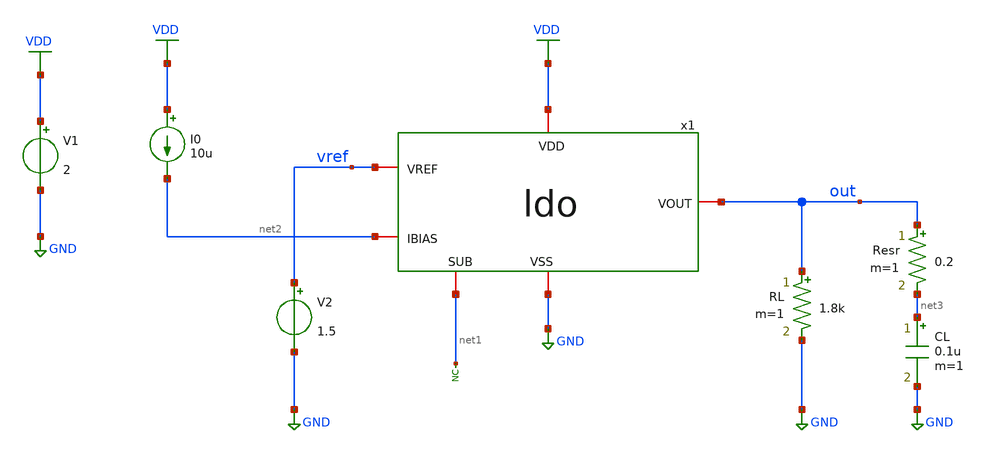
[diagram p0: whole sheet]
** sch_path: designs/libs/tb_ldo/tb_ldo/tb_ldo/tb_ldo_noise/tb_ldo_noise.sch
**.subckt tb_ldo_noise
* noconn #net1
RL out GND 1.8k m=1
V1 VDD GND 2
V2 vref GND 1.5
I0 VDD net2 10u
CL net3 GND 0.1u m=1
Resr out net3 0.2 m=1
x1 VDD vref out net2 net1 GND ldo
**** begin user architecture code



.control
save all

** Set sources
alter @V1[AC] = 1

** Simulation
op
noise v(out) V1 dec 100 1 10G

** Plots
setplot noise1
plot onoise_spectrum
plot inoise_spectrum

** Measurements
let output_noise_at_1MHz = onoise_spectrum[600]
print output_noise_at_1MHz

write tb_ldo_noise.raw
.endc
* ngspice commands




.include $::180MCU_MODELS/design.ngspice
.lib $::180MCU_MODELS/sm141064.ngspice typical
.lib $::180MCU_MODELS/sm141064.ngspice cap_mim
.lib $::180MCU_MODELS/sm141064.ngspice moscap_typical
.lib $::180MCU_MODELS/sm141064.ngspice mimcap_typical
.lib $::180MCU_MODELS/sm141064.ngspice res_typical
* .lib $::180MCU_MODELS/sm141064.ngspice res_statistical
* ngspice commands

**** end user architecture code
**.ends
.GLOBAL GND
.GLOBAL VDD
.end
